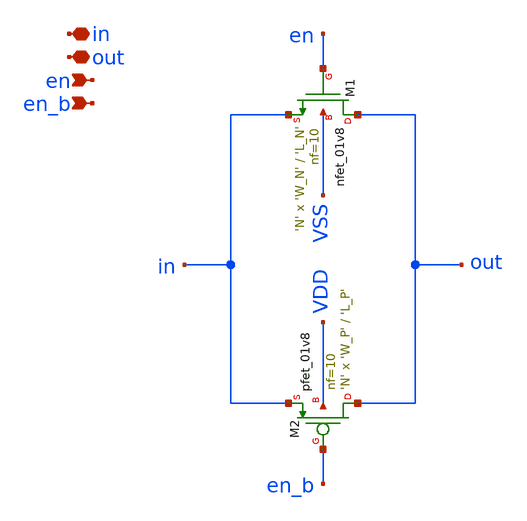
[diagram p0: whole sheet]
** sch_path: design/analog_modulator/schematic/transmission_gate.sch
**.subckt transmission_gate in out en en_b
*.iopin in
*.iopin out
*.ipin en
*.ipin en_b
XM1 out en in VSS sky130_fd_pr__nfet_01v8 L='L_N' W='W_N' nf=10 ad='int((nf+1)/2) * W/nf * 0.29' as='int((nf+2)/2) * W/nf * 0.29'
+ pd='2*int((nf+1)/2) * (W/nf + 0.29)' ps='2*int((nf+2)/2) * (W/nf + 0.29)' nrd='0.29 / W' nrs='0.29 / W'
+ sa=0 sb=0 sd=0 mult='N' m='N'
XM2 out en_b in VDD sky130_fd_pr__pfet_01v8 L='L_P' W='W_P' nf=10 ad='int((nf+1)/2) * W/nf * 0.29' as='int((nf+2)/2) * W/nf * 0.29'
+ pd='2*int((nf+1)/2) * (W/nf + 0.29)' ps='2*int((nf+2)/2) * (W/nf + 0.29)' nrd='0.29 / W' nrs='0.29 / W'
+ sa=0 sb=0 sd=0 mult='N' m='N'
**.ends
.end
